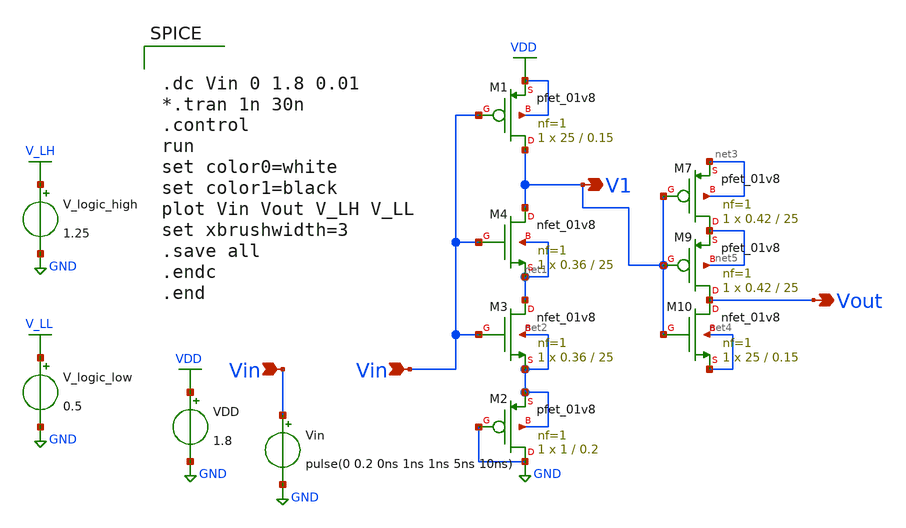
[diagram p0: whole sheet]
** sch_path: xschem/Vth_sch/th15.sch
**.subckt th15 Vin Vin V1 Vout
*.ipin Vin
*.ipin Vin
*.opin V1
*.opin Vout
VDD VDD GND 1.8
Vin Vin GND pulse(0 0.2 0ns 1ns 1ns 5ns 10ns)
XM1 V1 Vin VDD VDD sky130_fd_pr__pfet_01v8 L=0.15 W=25 nf=1 ad='int((nf+1)/2) * W/nf * 0.29' as='int((nf+2)/2) * W/nf * 0.29'
+ pd='2*int((nf+1)/2) * (W/nf + 0.29)' ps='2*int((nf+2)/2) * (W/nf + 0.29)' nrd='0.29 / W' nrs='0.29 / W'
+ sa=0 sb=0 sd=0 mult=1 m=1
V_logic_high V_LH GND 1.25
V_logic_low V_LL GND 0.5
XM3 net1 Vin net2 net2 sky130_fd_pr__nfet_01v8 L=25 W=0.36 nf=1 ad='int((nf+1)/2) * W/nf * 0.29' as='int((nf+2)/2) * W/nf * 0.29'
+ pd='2*int((nf+1)/2) * (W/nf + 0.29)' ps='2*int((nf+2)/2) * (W/nf + 0.29)' nrd='0.29 / W' nrs='0.29 / W'
+ sa=0 sb=0 sd=0 mult=1 m=1
XM4 V1 Vin net1 net1 sky130_fd_pr__nfet_01v8 L=25 W=0.36 nf=1 ad='int((nf+1)/2) * W/nf * 0.29' as='int((nf+2)/2) * W/nf * 0.29'
+ pd='2*int((nf+1)/2) * (W/nf + 0.29)' ps='2*int((nf+2)/2) * (W/nf + 0.29)' nrd='0.29 / W' nrs='0.29 / W'
+ sa=0 sb=0 sd=0 mult=1 m=1
XM2 GND GND net2 net2 sky130_fd_pr__pfet_01v8 L=0.2 W=1 nf=1 ad='int((nf+1)/2) * W/nf * 0.29' as='int((nf+2)/2) * W/nf * 0.29'
+ pd='2*int((nf+1)/2) * (W/nf + 0.29)' ps='2*int((nf+2)/2) * (W/nf + 0.29)' nrd='0.29 / W' nrs='0.29 / W'
+ sa=0 sb=0 sd=0 mult=1 m=1
XM7 net5 V1 net3 net3 sky130_fd_pr__pfet_01v8 L=25 W=0.42 nf=1 ad='int((nf+1)/2) * W/nf * 0.29' as='int((nf+2)/2) * W/nf * 0.29'
+ pd='2*int((nf+1)/2) * (W/nf + 0.29)' ps='2*int((nf+2)/2) * (W/nf + 0.29)' nrd='0.29 / W' nrs='0.29 / W'
+ sa=0 sb=0 sd=0 mult=1 m=1
XM9 Vout V1 net5 net5 sky130_fd_pr__pfet_01v8 L=25 W=0.42 nf=1 ad='int((nf+1)/2) * W/nf * 0.29' as='int((nf+2)/2) * W/nf * 0.29'
+ pd='2*int((nf+1)/2) * (W/nf + 0.29)' ps='2*int((nf+2)/2) * (W/nf + 0.29)' nrd='0.29 / W' nrs='0.29 / W'
+ sa=0 sb=0 sd=0 mult=1 m=1
XM10 Vout V1 net4 net4 sky130_fd_pr__nfet_01v8 L=0.15 W=25 nf=1 ad='int((nf+1)/2) * W/nf * 0.29' as='int((nf+2)/2) * W/nf * 0.29'
+ pd='2*int((nf+1)/2) * (W/nf + 0.29)' ps='2*int((nf+2)/2) * (W/nf + 0.29)' nrd='0.29 / W' nrs='0.29 / W'
+ sa=0 sb=0 sd=0 mult=1 m=1
**** begin user architecture code


.lib /usr/local/share/pdk/sky130A/libs.tech/ngspice/sky130.lib.spice tt

.save all





.dc Vin 0 1.8 0.01
*.tran 1n 30n
.control
run
set color0=white
set color1=black
plot Vin Vout V_LH V_LL
set xbrushwidth=3
.save all
.endc
.end


**** end user architecture code
**.ends
.GLOBAL VDD
.GLOBAL GND
.GLOBAL V_LH
.GLOBAL V_LL
.end
